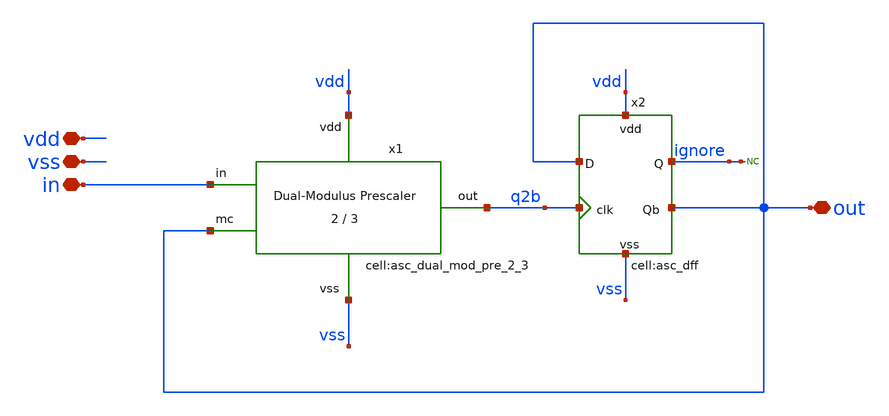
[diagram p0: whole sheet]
** sch_path: designs/libs/core_analog/asc_N_5_divider/asc_N_5_divider.sch
**.subckt asc_N_5_divider vdd vss in out
*.iopin vdd
*.iopin vss
*.iopin in
*.iopin out
x1 vdd vss q2b in out asc_dual_mod_pre_2_3
x2 q2b out out vdd vss ignore asc_dff
* noconn ignore
**.ends
.end
